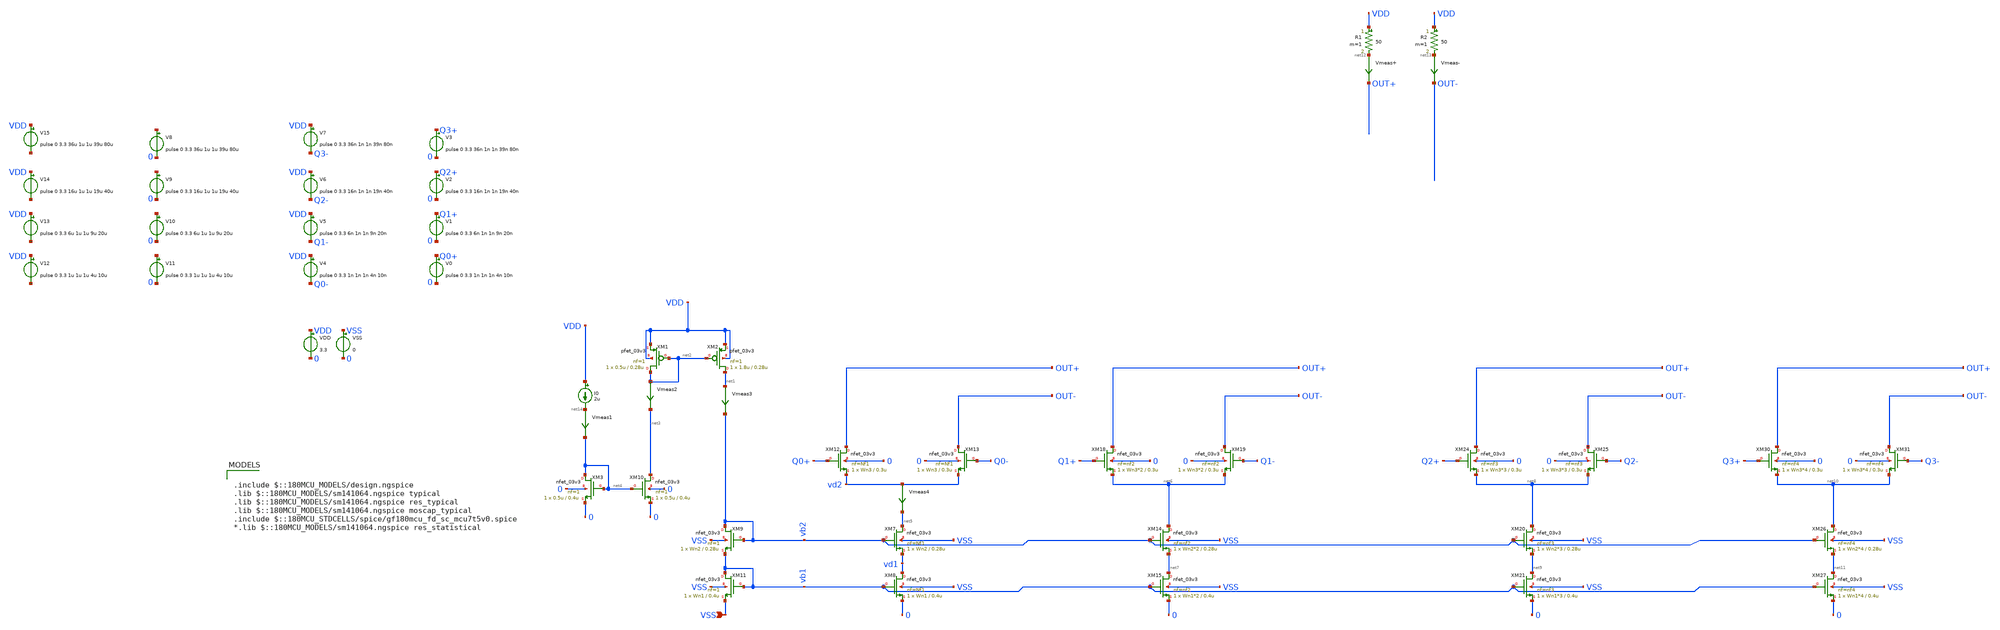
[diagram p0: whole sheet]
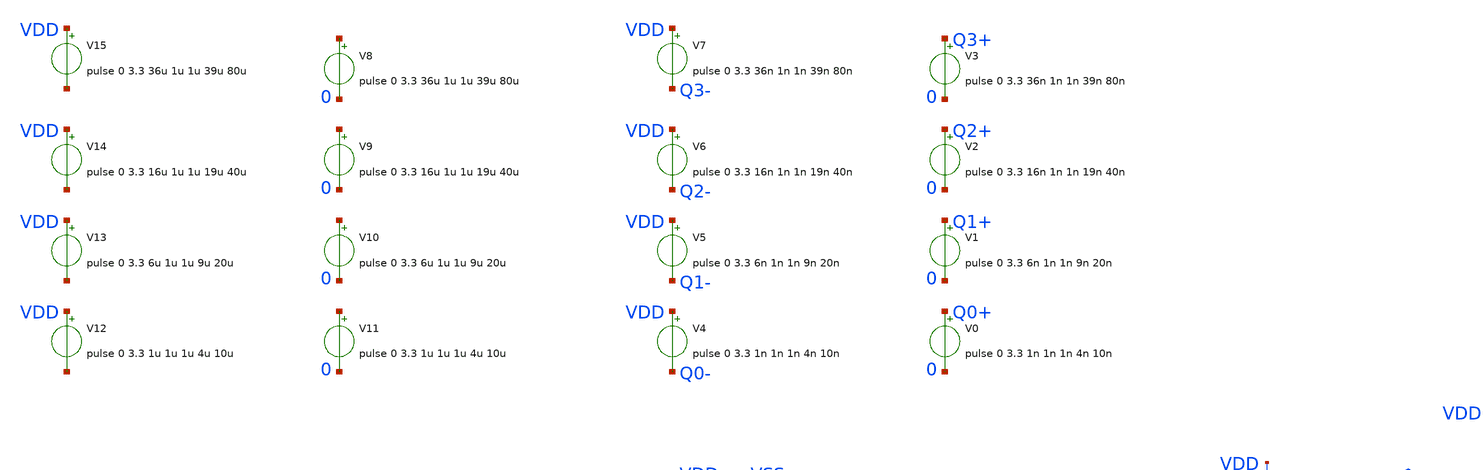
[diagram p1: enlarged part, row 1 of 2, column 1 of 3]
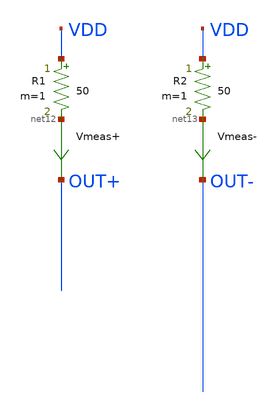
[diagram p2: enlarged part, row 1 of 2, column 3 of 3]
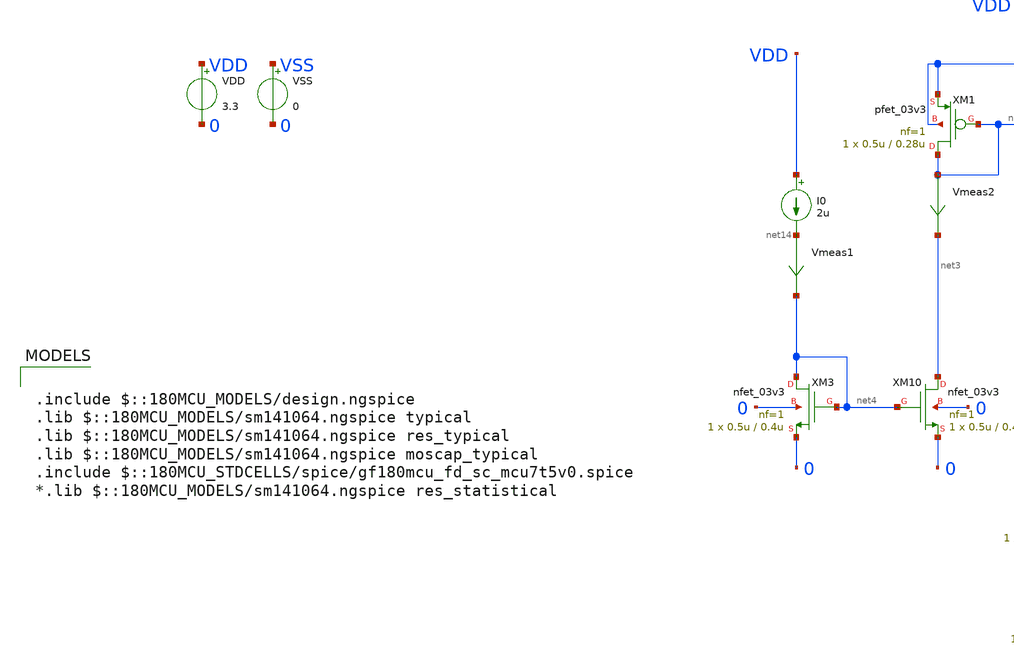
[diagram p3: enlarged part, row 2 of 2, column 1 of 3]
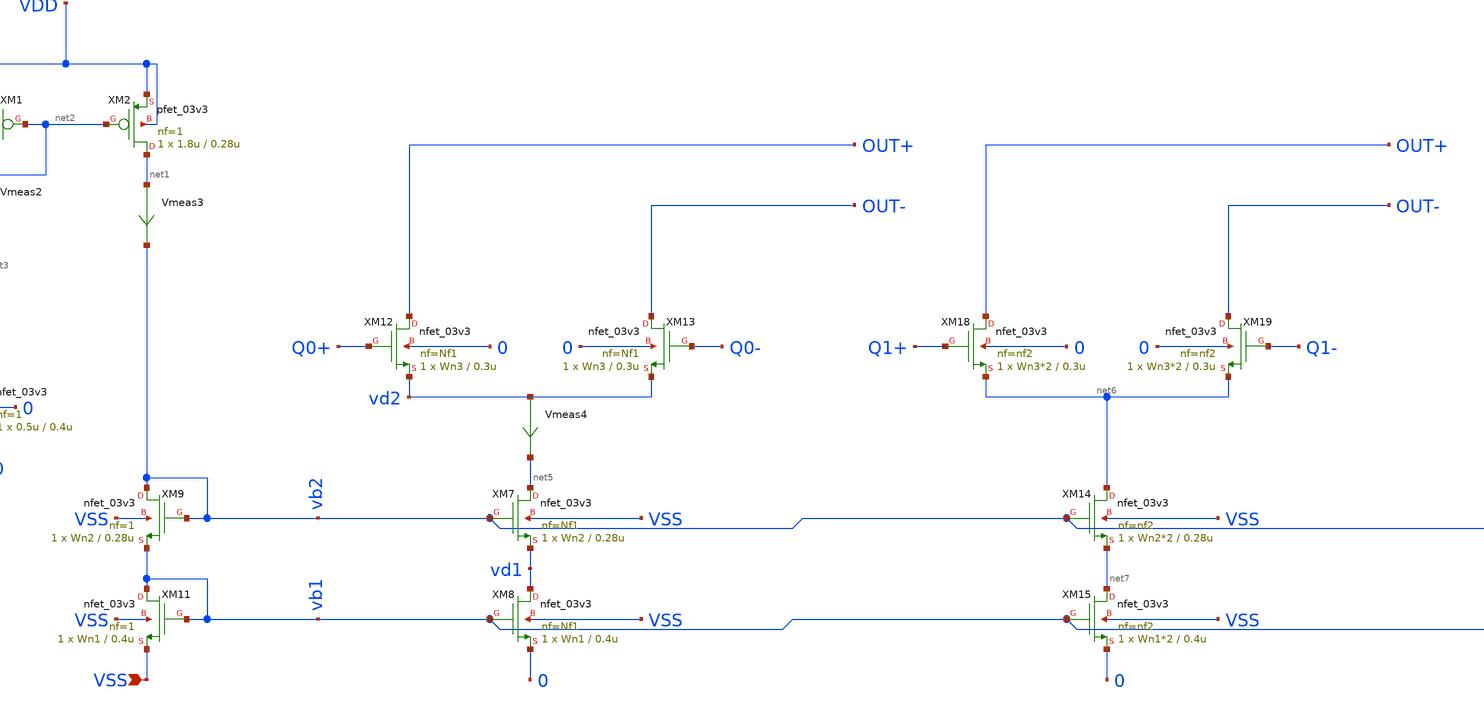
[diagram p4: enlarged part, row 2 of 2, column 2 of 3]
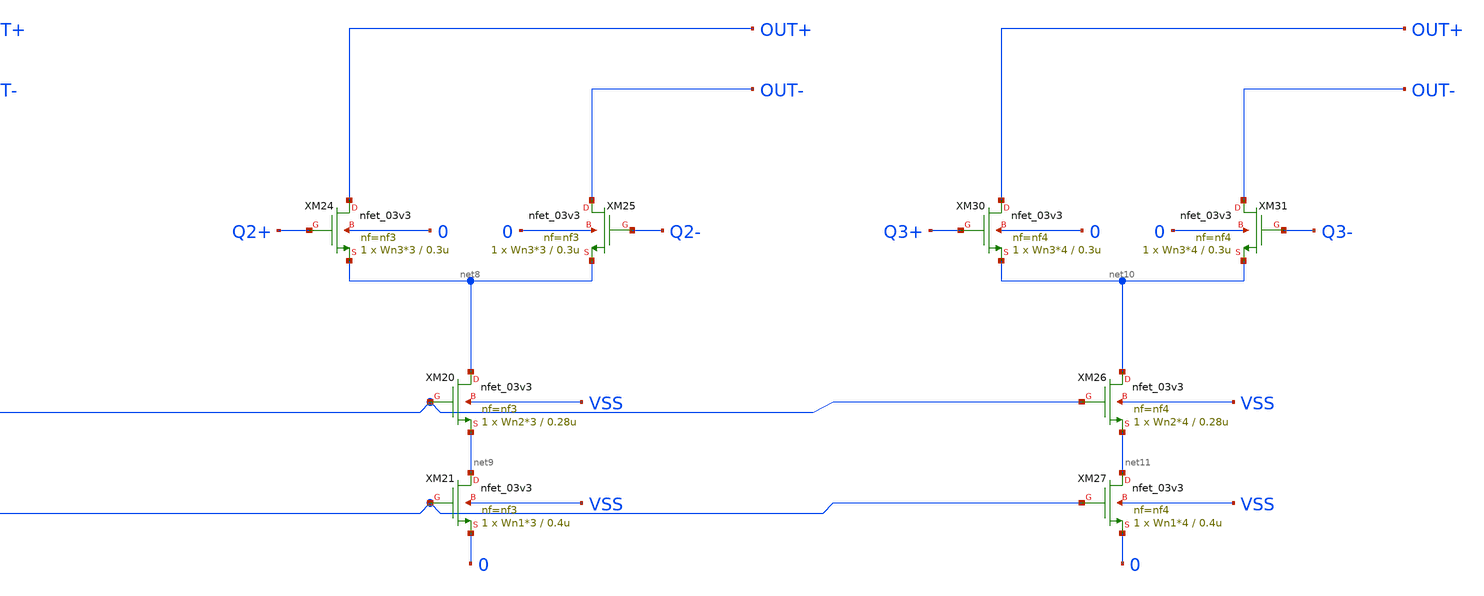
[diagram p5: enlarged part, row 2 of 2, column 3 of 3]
** sch_path: xschem/untitled.sch
**.subckt untitled VSS
*.ipin VSS
R1 VDD net12 50 m=1
R2 VDD net13 50 m=1
Vmeas+ net12 OUT+ 0
.save i(vmeas+)
Vmeas- net13 OUT- 0
.save i(vmeas-)
VDD VDD 0 3.3
VSS VSS 0 0
XM1 net2 net2 VDD VDD pfet_03v3 L=0.28u W=0.5u nf=1 ad='int((nf+1)/2) * W/nf * 0.18u' as='int((nf+2)/2) * W/nf * 0.18u'
+ pd='2*int((nf+1)/2) * (W/nf + 0.18u)' ps='2*int((nf+2)/2) * (W/nf + 0.18u)' nrd='0.18u / W' nrs='0.18u / W'
+ sa=0 sb=0 sd=0 m=1
XM2 net1 net2 VDD VDD pfet_03v3 L=0.28u W=1.8u nf=1 ad='int((nf+1)/2) * W/nf * 0.18u' as='int((nf+2)/2) * W/nf * 0.18u'
+ pd='2*int((nf+1)/2) * (W/nf + 0.18u)' ps='2*int((nf+2)/2) * (W/nf + 0.18u)' nrd='0.18u / W' nrs='0.18u / W'
+ sa=0 sb=0 sd=0 m=1
I0 VDD net14 2u
XM3 net4 net4 0 0 nfet_03v3 L=0.4u W=0.5u nf=1 ad='int((nf+1)/2) * W/nf * 0.18u' as='int((nf+2)/2) * W/nf * 0.18u'
+ pd='2*int((nf+1)/2) * (W/nf + 0.18u)' ps='2*int((nf+2)/2) * (W/nf + 0.18u)' nrd='0.18u / W' nrs='0.18u / W'
+ sa=0 sb=0 sd=0 m=1
XM10 net3 net4 0 0 nfet_03v3 L=0.4u W=0.5u nf=1 ad='int((nf+1)/2) * W/nf * 0.18u' as='int((nf+2)/2) * W/nf * 0.18u'
+ pd='2*int((nf+1)/2) * (W/nf + 0.18u)' ps='2*int((nf+2)/2) * (W/nf + 0.18u)' nrd='0.18u / W' nrs='0.18u / W'
+ sa=0 sb=0 sd=0 m=1
Vmeas1 net14 net4 0
.save i(vmeas1)
XM7 net5 vb2 vd1 VSS nfet_03v3 L=0.28u W=Wn2 nf=Nf1 ad='int((nf+1)/2) * W/nf * 0.18u' as='int((nf+2)/2) * W/nf * 0.18u'
+ pd='2*int((nf+1)/2) * (W/nf + 0.18u)' ps='2*int((nf+2)/2) * (W/nf + 0.18u)' nrd='0.18u / W' nrs='0.18u / W'
+ sa=0 sb=0 sd=0 m=1
XM8 vd1 vb1 0 VSS nfet_03v3 L=0.4u W=Wn1 nf=Nf1 ad='int((nf+1)/2) * W/nf * 0.18u' as='int((nf+2)/2) * W/nf * 0.18u'
+ pd='2*int((nf+1)/2) * (W/nf + 0.18u)' ps='2*int((nf+2)/2) * (W/nf + 0.18u)' nrd='0.18u / W' nrs='0.18u / W'
+ sa=0 sb=0 sd=0 m=1
XM9 vb2 vb2 vb1 VSS nfet_03v3 L=0.28u W=Wn2 nf=1 ad='int((nf+1)/2) * W/nf * 0.18u' as='int((nf+2)/2) * W/nf * 0.18u'
+ pd='2*int((nf+1)/2) * (W/nf + 0.18u)' ps='2*int((nf+2)/2) * (W/nf + 0.18u)' nrd='0.18u / W' nrs='0.18u / W'
+ sa=0 sb=0 sd=0 m=1
XM11 vb1 vb1 VSS VSS nfet_03v3 L=0.4u W=Wn1 nf=1 ad='int((nf+1)/2) * W/nf * 0.18u' as='int((nf+2)/2) * W/nf * 0.18u'
+ pd='2*int((nf+1)/2) * (W/nf + 0.18u)' ps='2*int((nf+2)/2) * (W/nf + 0.18u)' nrd='0.18u / W' nrs='0.18u / W'
+ sa=0 sb=0 sd=0 m=1
XM12 OUT+ Q0+ vd2 0 nfet_03v3 L=0.3u W=Wn3 nf=Nf1 ad='int((nf+1)/2) * W/nf * 0.18u' as='int((nf+2)/2) * W/nf * 0.18u'
+ pd='2*int((nf+1)/2) * (W/nf + 0.18u)' ps='2*int((nf+2)/2) * (W/nf + 0.18u)' nrd='0.18u / W' nrs='0.18u / W'
+ sa=0 sb=0 sd=0 m=1
XM13 OUT- Q0- vd2 0 nfet_03v3 L=0.3u W=Wn3 nf=Nf1 ad='int((nf+1)/2) * W/nf * 0.18u' as='int((nf+2)/2) * W/nf * 0.18u'
+ pd='2*int((nf+1)/2) * (W/nf + 0.18u)' ps='2*int((nf+2)/2) * (W/nf + 0.18u)' nrd='0.18u / W' nrs='0.18u / W'
+ sa=0 sb=0 sd=0 m=1
Vmeas2 net2 net3 0
.save i(vmeas2)
XM14 net6 vb2 net7 VSS nfet_03v3 L=0.28u W=Wn2*2 nf=nf2 ad='int((nf+1)/2) * W/nf * 0.18u' as='int((nf+2)/2) * W/nf * 0.18u'
+ pd='2*int((nf+1)/2) * (W/nf + 0.18u)' ps='2*int((nf+2)/2) * (W/nf + 0.18u)' nrd='0.18u / W' nrs='0.18u / W'
+ sa=0 sb=0 sd=0 m=1
XM15 net7 vb1 0 VSS nfet_03v3 L=0.4u W=Wn1*2 nf=nf2 ad='int((nf+1)/2) * W/nf * 0.18u' as='int((nf+2)/2) * W/nf * 0.18u'
+ pd='2*int((nf+1)/2) * (W/nf + 0.18u)' ps='2*int((nf+2)/2) * (W/nf + 0.18u)' nrd='0.18u / W' nrs='0.18u / W'
+ sa=0 sb=0 sd=0 m=1
XM18 OUT+ Q1+ net6 0 nfet_03v3 L=0.3u W=Wn3*2 nf=nf2 ad='int((nf+1)/2) * W/nf * 0.18u' as='int((nf+2)/2) * W/nf * 0.18u'
+ pd='2*int((nf+1)/2) * (W/nf + 0.18u)' ps='2*int((nf+2)/2) * (W/nf + 0.18u)' nrd='0.18u / W' nrs='0.18u / W'
+ sa=0 sb=0 sd=0 m=1
XM19 OUT- Q1- net6 0 nfet_03v3 L=0.3u W=Wn3*2 nf=nf2 ad='int((nf+1)/2) * W/nf * 0.18u' as='int((nf+2)/2) * W/nf * 0.18u'
+ pd='2*int((nf+1)/2) * (W/nf + 0.18u)' ps='2*int((nf+2)/2) * (W/nf + 0.18u)' nrd='0.18u / W' nrs='0.18u / W'
+ sa=0 sb=0 sd=0 m=1
XM20 net8 vb2 net9 VSS nfet_03v3 L=0.28u W=Wn2*3 nf=nf3 ad='int((nf+1)/2) * W/nf * 0.18u' as='int((nf+2)/2) * W/nf * 0.18u'
+ pd='2*int((nf+1)/2) * (W/nf + 0.18u)' ps='2*int((nf+2)/2) * (W/nf + 0.18u)' nrd='0.18u / W' nrs='0.18u / W'
+ sa=0 sb=0 sd=0 m=1
XM21 net9 vb1 0 VSS nfet_03v3 L=0.4u W=Wn1*3 nf=nf3 ad='int((nf+1)/2) * W/nf * 0.18u' as='int((nf+2)/2) * W/nf * 0.18u'
+ pd='2*int((nf+1)/2) * (W/nf + 0.18u)' ps='2*int((nf+2)/2) * (W/nf + 0.18u)' nrd='0.18u / W' nrs='0.18u / W'
+ sa=0 sb=0 sd=0 m=1
XM24 OUT+ Q2+ net8 0 nfet_03v3 L=0.3u W=Wn3*3 nf=nf3 ad='int((nf+1)/2) * W/nf * 0.18u' as='int((nf+2)/2) * W/nf * 0.18u'
+ pd='2*int((nf+1)/2) * (W/nf + 0.18u)' ps='2*int((nf+2)/2) * (W/nf + 0.18u)' nrd='0.18u / W' nrs='0.18u / W'
+ sa=0 sb=0 sd=0 m=1
XM25 OUT- Q2- net8 0 nfet_03v3 L=0.3u W=Wn3*3 nf=nf3 ad='int((nf+1)/2) * W/nf * 0.18u' as='int((nf+2)/2) * W/nf * 0.18u'
+ pd='2*int((nf+1)/2) * (W/nf + 0.18u)' ps='2*int((nf+2)/2) * (W/nf + 0.18u)' nrd='0.18u / W' nrs='0.18u / W'
+ sa=0 sb=0 sd=0 m=1
XM26 net10 vb2 net11 VSS nfet_03v3 L=0.28u W=Wn2*4 nf=nf4 ad='int((nf+1)/2) * W/nf * 0.18u' as='int((nf+2)/2) * W/nf * 0.18u'
+ pd='2*int((nf+1)/2) * (W/nf + 0.18u)' ps='2*int((nf+2)/2) * (W/nf + 0.18u)' nrd='0.18u / W' nrs='0.18u / W'
+ sa=0 sb=0 sd=0 m=1
XM27 net11 vb1 0 VSS nfet_03v3 L=0.4u W=Wn1*4 nf=nf4 ad='int((nf+1)/2) * W/nf * 0.18u' as='int((nf+2)/2) * W/nf * 0.18u'
+ pd='2*int((nf+1)/2) * (W/nf + 0.18u)' ps='2*int((nf+2)/2) * (W/nf + 0.18u)' nrd='0.18u / W' nrs='0.18u / W'
+ sa=0 sb=0 sd=0 m=1
XM30 OUT+ Q3+ net10 0 nfet_03v3 L=0.3u W=Wn3*4 nf=nf4 ad='int((nf+1)/2) * W/nf * 0.18u' as='int((nf+2)/2) * W/nf * 0.18u'
+ pd='2*int((nf+1)/2) * (W/nf + 0.18u)' ps='2*int((nf+2)/2) * (W/nf + 0.18u)' nrd='0.18u / W' nrs='0.18u / W'
+ sa=0 sb=0 sd=0 m=1
XM31 OUT- Q3- net10 0 nfet_03v3 L=0.3u W=Wn3*4 nf=nf4 ad='int((nf+1)/2) * W/nf * 0.18u' as='int((nf+2)/2) * W/nf * 0.18u'
+ pd='2*int((nf+1)/2) * (W/nf + 0.18u)' ps='2*int((nf+2)/2) * (W/nf + 0.18u)' nrd='0.18u / W' nrs='0.18u / W'
+ sa=0 sb=0 sd=0 m=1
V2 Q2+ 0 pulse 0 3.3 16n 1n 1n 19n 40n
V1 Q1+ 0 pulse 0 3.3 6n 1n 1n 9n 20n
V0 Q0+ 0 pulse 0 3.3 1n 1n 1n 4n 10n
V3 Q3+ 0 pulse 0 3.3 36n 1n 1n 39n 80n
V4 VDD Q0- pulse 0 3.3 1n 1n 1n 4n 10n
V5 VDD Q1- pulse 0 3.3 6n 1n 1n 9n 20n
V6 VDD Q2- pulse 0 3.3 16n 1n 1n 19n 40n
V7 VDD Q3- pulse 0 3.3 36n 1n 1n 39n 80n
V12 VDD net15 pulse 0 3.3 1u 1u 1u 4u 10u
V13 VDD net16 pulse 0 3.3 6u 1u 1u 9u 20u
V14 VDD net17 pulse 0 3.3 16u 1u 1u 19u 40u
V15 VDD net18 pulse 0 3.3 36u 1u 1u 39u 80u
V8 net19 0 pulse 0 3.3 36u 1u 1u 39u 80u
V9 net20 0 pulse 0 3.3 16u 1u 1u 19u 40u
V10 net21 0 pulse 0 3.3 6u 1u 1u 9u 20u
V11 net22 0 pulse 0 3.3 1u 1u 1u 4u 10u
Vmeas3 net1 vb2 0
.save i(vmeas3)
Vmeas4 vd2 net5 0
.save i(vmeas4)
**** begin user architecture code


.param Mn1=1
.param Mn2=1
.param Mn3=1
.param Mn4=1
.param Nf1=1
.param Nf2=2
.param Nf3=3
.param Nf4=4

.param Wn1=0.8u
.param Wn2=0.6u
.param Wn3=0.6u
.save @m.xm7.m0[vth] @m.xm8.m0[vth] @m.xm27.m0[vth] @m.xm26.m0[vth] @m.xm30.m0[vth]
.options savecurrents

.control
	tran 0.5n 10n
	*plot i(Vmeas1) i(Vmeas2) i(Vmeas3) i(Vmeas4)
	*plot v(vb2) v(vb1) v(vd1) v(vd2)
	*plot i(Vmeas+) i(Vmeas-)
	plot v(vb1)-@m.xm8.m0[vth]
	plot v(vb2)-v(vd1)-@m.xm7.m0[vth]
	plot v(q0+)-v(vd2)-@m.xm12.m0[vth]
	plot @m.xm26.m0[vth] @m.xm27.m0[vth] @m.xm30.m0[vth]
	write test_dac_LSB_matrix.raw
.endc

.save all



.include $::180MCU_MODELS/design.ngspice
.lib $::180MCU_MODELS/sm141064.ngspice typical
.lib $::180MCU_MODELS/sm141064.ngspice res_typical
.lib $::180MCU_MODELS/sm141064.ngspice moscap_typical
.include $::180MCU_STDCELLS/spice/gf180mcu_fd_sc_mcu7t5v0.spice
*.lib $::180MCU_MODELS/sm141064.ngspice res_statistical

**** end user architecture code
**.ends
.end
